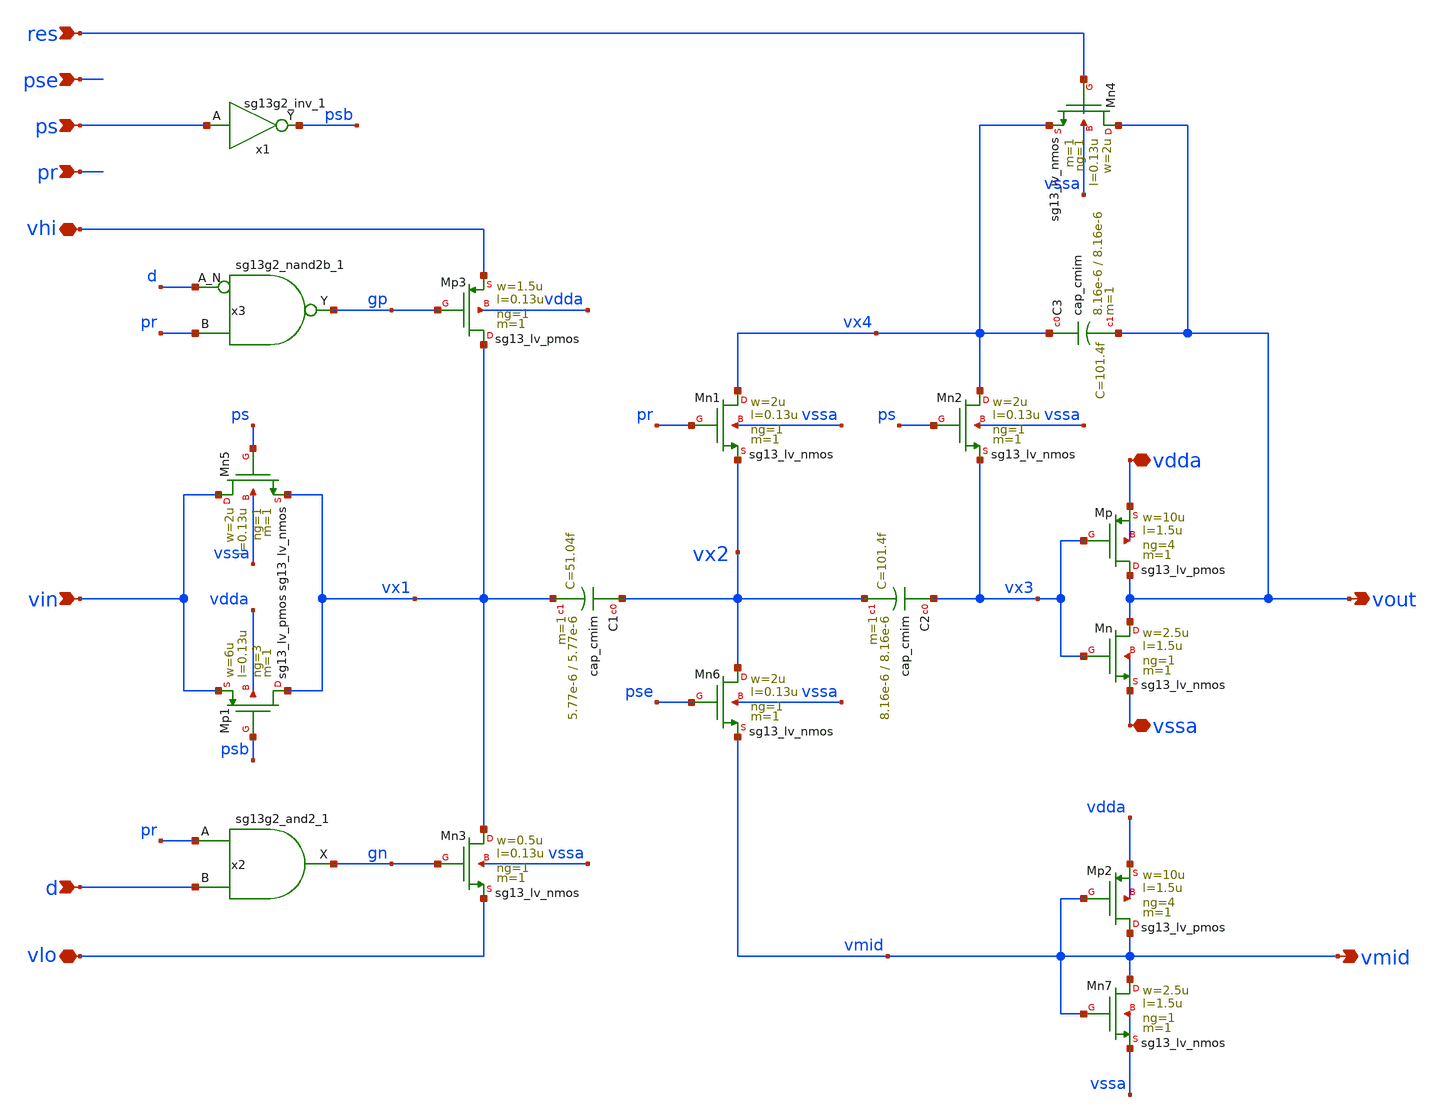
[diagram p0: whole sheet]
** sch_path: 5_Design/3_Real_circuits/template_stage.sch
* IHP-GmbH/IHP-Open-PDK/ihp-sg13g2/libs.tech/xschem/sg13g2_stdcells/sg13g2_nand2b_1.sch:
* Copyright 2023 IHP PDK Authors
* Licensed under the Apache License, Version 2.0 (the "License");
**.subckt template_stage vout vdda res vin pse ps pr d vssa vhi vlo vmid
*.opin vout
*.iopin vdda
*.ipin res
*.ipin vin
*.ipin pse
*.ipin ps
*.ipin pr
*.ipin d
*.iopin vssa
*.iopin vhi
*.iopin vlo
*.opin vmid
XMn vout vx3 vssa vssa sg13_lv_nmos w=2.5u l=1.5u ng=1 m=1 mm_ok=1
XMp vout vx3 vdda vdda sg13_lv_pmos w=10u l=1.5u ng=4 m=1 mm_ok=1
XMn3 vx1 gn vlo vssa sg13_lv_nmos w=0.5u l=0.13u ng=1 m=1 mm_ok=1
XMn4 vout res vx4 vssa sg13_lv_nmos w=2u l=0.13u ng=1 m=1 mm_ok=1
x1 psb ps VDD VSS sg13g2_inv_1
XMp1 vx1 psb vin vdda sg13_lv_pmos w=6u l=0.13u ng=3 m=1 mm_ok=1
XMn5 vin ps vx1 vssa sg13_lv_nmos w=2u l=0.13u ng=1 m=1 mm_ok=1
XMn1 vx4 pr vx2 vssa sg13_lv_nmos w=2u l=0.13u ng=1 m=1 mm_ok=1
XMn2 vx4 ps vx3 vssa sg13_lv_nmos w=2u l=0.13u ng=1 m=1 mm_ok=1
XMn7 vmid vmid vssa vssa sg13_lv_nmos w=2.5u l=1.5u ng=1 m=1 mm_ok=1
XMp2 vmid vmid vdda vdda sg13_lv_pmos w=10u l=1.5u ng=4 m=1 mm_ok=1
x2 gn pr d VDD VSS sg13g2_and2_1
XMp3 vx1 gp vhi vdda sg13_lv_pmos w=1.5u l=0.13u ng=1 m=1 mm_ok=1
x3 gp d pr VDD VSS sg13g2_nand2b_1
XC1 vx2 vx1 cap_cmim w=5.77e-6 l=5.77e-6 m=1 mm_ok=1
XC2 vx3 vx2 cap_cmim w=8.16e-6 l=8.16e-6 m=1 mm_ok=1
XC3 vx4 vout cap_cmim w=8.16e-6 l=8.16e-6 m=1 mm_ok=1
XMn6 vx2 pse vmid vssa sg13_lv_nmos w=2u l=0.13u ng=1 m=1 mm_ok=1
**.ends

* expanding   symbol:  sg13g2_stdcells/sg13g2_inv_1.sym # of pins=2
** sym_path: sg13g2_stdcells/sg13g2_inv_1.sym
** sch_path: sg13g2_stdcells/sg13g2_inv_1.sch
.subckt sg13g2_inv_1 Y A VDD VSS
*.opin Y
*.ipin A
*.iopin VDD
*.iopin VSS
XM1 Y A VSS VSS sg13_lv_nmos w=740.00n l=130.00n ng=1 m=1 mm_ok=1
XM2 Y A VDD VDD sg13_lv_pmos w=1.12u l=130.00n ng=1 m=1 mm_ok=1
.ends


* expanding   symbol:  sg13g2_stdcells/sg13g2_and2_1.sym # of pins=3
** sym_path: sg13g2_stdcells/sg13g2_and2_1.sym
** sch_path: sg13g2_stdcells/sg13g2_and2_1.sch
.subckt sg13g2_and2_1 X A B VDD VSS
*.ipin A
*.ipin B
*.opin X
*.iopin VDD
*.iopin VSS
XM1 net1 A net2 VSS sg13_lv_nmos w=640.00n l=130.00n ng=1 m=1 mm_ok=1
XM2 net2 B VSS VSS sg13_lv_nmos w=640.00n l=130.00n ng=1 m=1 mm_ok=1
XM3 X net1 VSS VSS sg13_lv_nmos w=740.00n l=130.00n ng=1 m=1 mm_ok=1
XM4 net1 B VDD VDD sg13_lv_pmos w=840.00n l=130.00n ng=1 m=1 mm_ok=1
XM5 net1 A VDD VDD sg13_lv_pmos w=840.00n l=130.00n ng=1 m=1 mm_ok=1
XM6 X net1 VDD VDD sg13_lv_pmos w=1.12u l=130.00n ng=1 m=1 mm_ok=1
.ends


* expanding   symbol:  sg13g2_stdcells/sg13g2_nand2b_1.sym # of pins=3
** sym_path: sg13g2_stdcells/sg13g2_nand2b_1.sym
** sch_path: sg13g2_stdcells/sg13g2_nand2b_1.sch
.subckt sg13g2_nand2b_1 Y A_N B VDD VSS
*.opin Y
*.ipin B
*.ipin A_N
*.iopin VDD
*.iopin VSS
XM1 net1 A_N VSS VSS sg13_lv_nmos w=550.00n l=130.00n ng=1 m=1 mm_ok=1
XM2 Y net1 net2 VSS sg13_lv_nmos w=740.00n l=130.00n ng=1 m=1 mm_ok=1
XM3 net2 B VSS VSS sg13_lv_nmos w=740.00n l=130.00n ng=1 m=1 mm_ok=1
XM4 Y B VDD VDD sg13_lv_pmos w=1.12u l=130.00n ng=1 m=1 mm_ok=1
XM5 net1 A_N VDD VDD sg13_lv_pmos w=840.00n l=130.00n ng=1 m=1 mm_ok=1
XM6 Y net1 VDD VDD sg13_lv_pmos w=1.12u l=130.00n ng=1 m=1 mm_ok=1
.ends

.end
